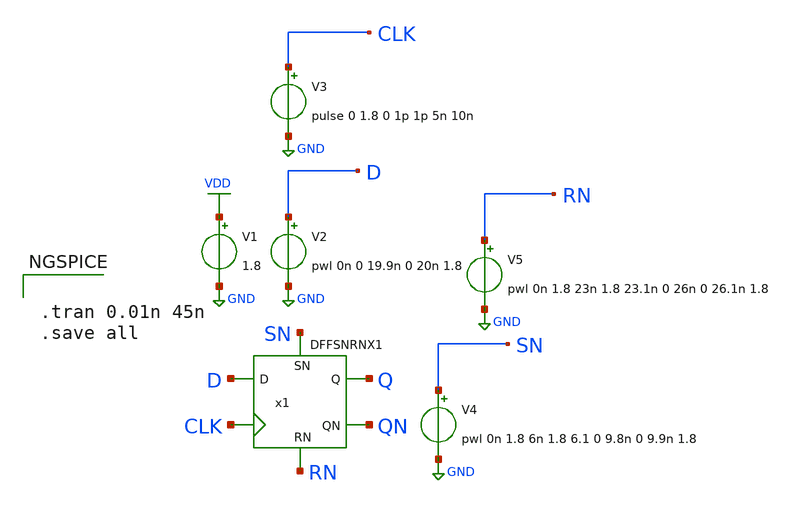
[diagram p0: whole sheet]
** sch_path: archives/lib/xschem/test_DFFSNRNX1.sch
**.subckt test_DFFSNRNX1
V2 D GND pwl 0n 0 19.9n 0 20n 1.8
V1 VDD GND 1.8
V3 CLK GND pulse 0 1.8 0 1p 1p 5n 10n
V4 SN GND pwl 0n 1.8 6n 1.8 6.1 0 9.8n 0 9.9n 1.8
V5 RN GND pwl 0n 1.8 23n 1.8 23.1n 0 26n 0 26.1n 1.8
x1 Q QN D CLK SN RN VDD GND DFFSNRNX1
**** begin user architecture code

.lib $::SKYWATER_MODELS/sky130.lib.spice tt


**** end user architecture code
**.ends
.GLOBAL VDD
.GLOBAL GND
**** begin user architecture code


.tran 0.01n 45n
.save all


**** end user architecture code
.end
